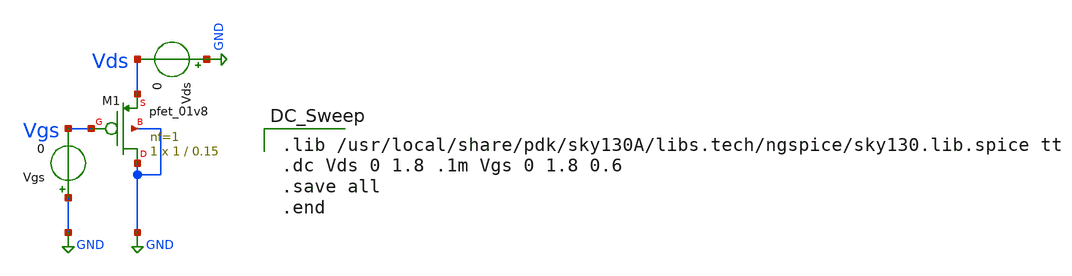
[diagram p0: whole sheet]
** sch_path: MOS/PMOS/Schematic/pmos.sch
**.subckt pmos
Vgs GND Vgs 0
Vds GND Vds 0
XM1 GND Vgs Vds GND sky130_fd_pr__pfet_01v8 L=0.15 W=1 nf=1 ad='int((nf+1)/2) * W/nf * 0.29' as='int((nf+2)/2) * W/nf * 0.29'
+ pd='2*int((nf+1)/2) * (W/nf + 0.29)' ps='2*int((nf+2)/2) * (W/nf + 0.29)' nrd='0.29 / W' nrs='0.29 / W'
+ sa=0 sb=0 sd=0 mult=1 m=1
**** begin user architecture code

.lib /usr/local/share/pdk/sky130A/libs.tech/ngspice/sky130.lib.spice tt
.dc Vds 0 1.8 .1m Vgs 0 1.8 0.6
.save all
.end

**** end user architecture code
**.ends
.GLOBAL GND
.end
